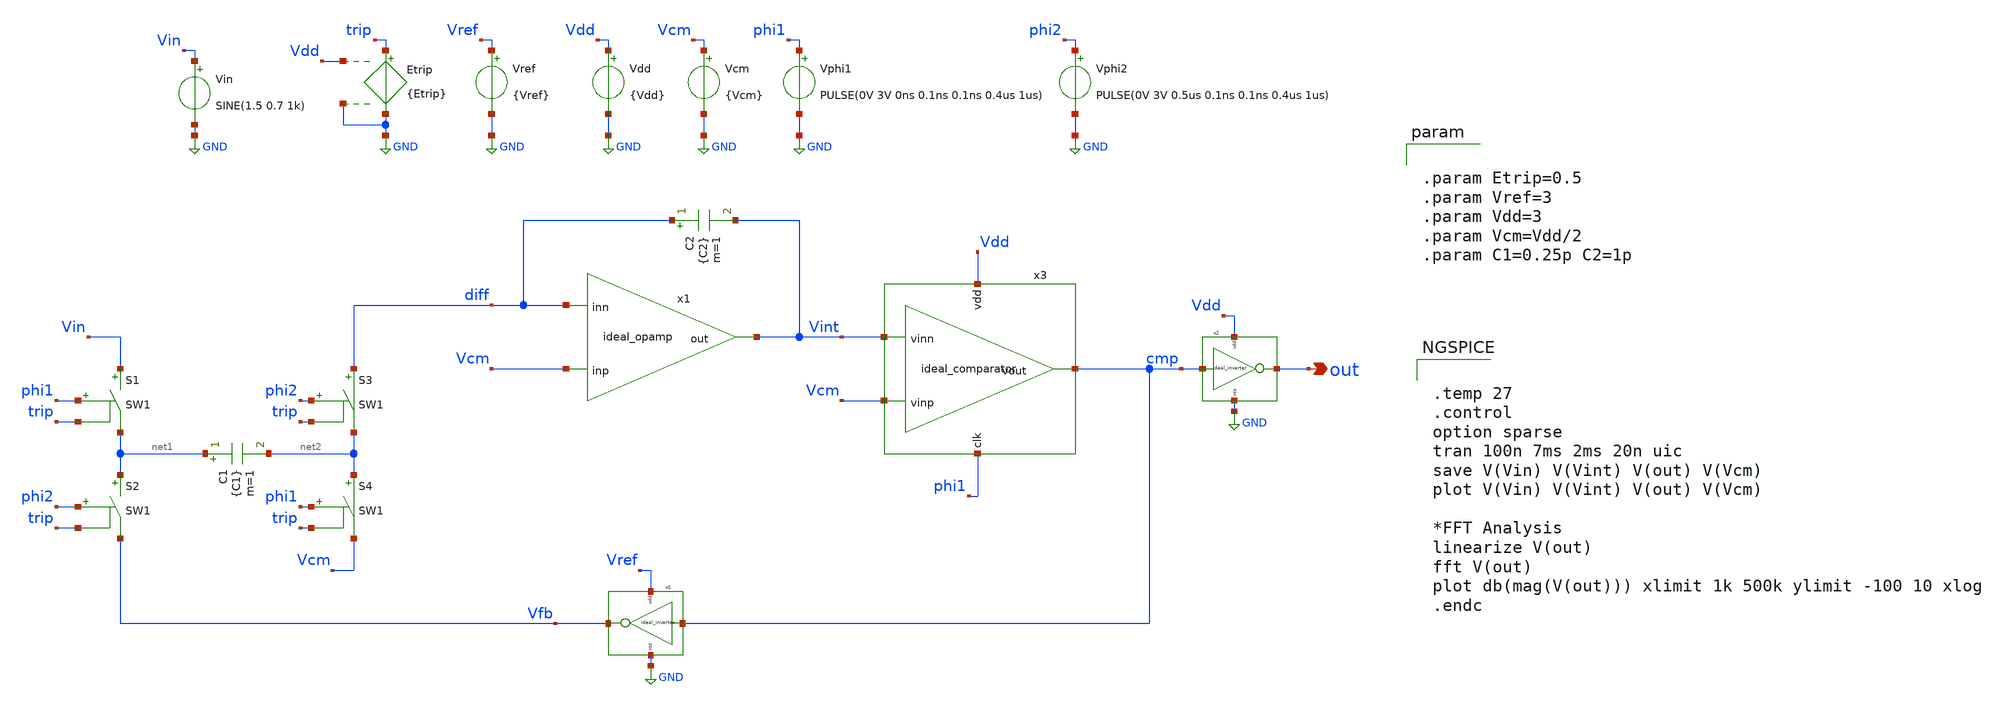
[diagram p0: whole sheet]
** sch_path: 2_ideal_circuits/modulator_tb.sch
**.subckt modulator_tb out
*.opin out
S1 Vin net1 phi1 trip SW1
S2 net1 Vfb phi2 trip SW1
S3 diff net2 phi2 trip SW1
S4 net2 Vcm phi1 trip SW1
x1 Vcm diff Vint ideal_opamp
C2 diff Vint {C2} m=1
Vin Vin GND SINE(1.5 0.7 1k)
Vref Vref GND {Vref}
Vdd Vdd GND {Vdd}
Vcm Vcm GND {Vcm}
Vphi1 phi1 GND PULSE(0V 3V 0ns 0.1ns 0.1ns 0.4us 1us)
Vphi2 phi2 GND PULSE(0V 3V 0.5us 0.1ns 0.1ns 0.4us 1us)
Etrip trip GND Vdd GND {Etrip}
C1 net1 net2 {C1} m=1
x3 Vdd cmp Vint Vcm phi1 ideal_comparator
x5 Vfb cmp GND Vref ideal_inverter
x2 out cmp GND Vdd ideal_inverter
**** begin user architecture code


.param Etrip=0.5
.param Vref=3
.param Vdd=3
.param Vcm=Vdd/2
.param C1=0.25p C2=1p




.temp 27
.control
option sparse
tran 100n 7ms 2ms 20n uic
save V(Vin) V(Vint) V(out) V(Vcm)
plot V(Vin) V(Vint) V(out) V(Vcm)

*FFT Analysis
linearize V(out)
fft V(out)
plot db(mag(V(out))) xlimit 1k 500k ylimit -100 10 xlog
.endc


**** end user architecture code
**.ends

* expanding   symbol:  ideal_opamp.sym # of pins=3
** sym_path: ideal_opamp.sym
** sch_path: ideal_opamp.sch
.subckt ideal_opamp inp inn out
*.opin out
*.ipin inp
*.ipin inn
E1 out GND inp inn 1Meg
R1 out GND 100Meg m=1
.ends


* expanding   symbol:  ideal_comparator.sym # of pins=5
** sym_path: 2_ideal_circuits/ideal_comparator.sym
** sch_path: 2_ideal_circuits/ideal_comparator.sch
.subckt ideal_comparator Vdd Vout Vinn Vinp clk
*.ipin Vinp
*.ipin Vinn
*.opin Vout
*.iopin Vdd
*.iopin clk
E1 diff GND Vinp Vinn 1
S1 diff sample tp clk SW1
E2 net1 GND sample GND 1
C1 sample GND 100p m=1
S2 net1 hold clk tp SW1
C2 hold GND 100p m=1
B1 Vout GND V={v(hold)>0?v(Vdd):0}
Etp tp GND Vdd GND 0.5
**** begin user architecture code


.ic v(hold)=1 v(sample)=1


**** end user architecture code
.ends


* expanding   symbol:  ideal_inverter.sym # of pins=4
** sym_path: 2_ideal_circuits/ideal_inverter.sym
** sch_path: 2_ideal_circuits/ideal_inverter.sch
.subckt ideal_inverter out in vss vdd
*.iopin vdd
*.ipin in
*.opin out
*.iopin vss
B1 out GND V={v(in)>v(vdd)/2?v(vss):v(vdd)}
* noconn vdd
* noconn in
* noconn vss
.ends

.GLOBAL GND
**** begin user architecture code
.MODEL SW1 SW( VT=0.9 VH=0.01 RON=0.01 ROFF=10G )
**** end user architecture code
.end
